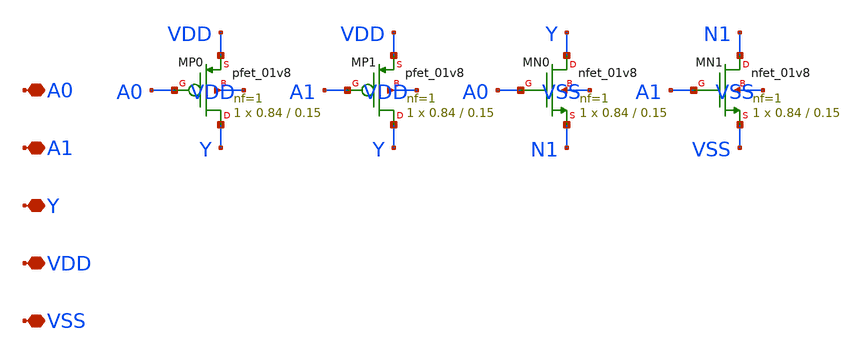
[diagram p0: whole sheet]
** sch_path: design/compiler/cells/sram_nand2.sch
**.subckt sram_nand2 A0 A1 Y VDD VSS
*.iopin A0
*.iopin A1
*.iopin Y
*.iopin VDD
*.iopin VSS
XMP0 Y A0 VDD VDD sky130_fd_pr__pfet_01v8 L=0.15 W=0.84 nf=1 ad=0.2436 as=0.2436 pd=2.26 ps=2.26
+ nrd=0.3452 nrs=0.3452 sa=0 sb=0 sd=0 mult=1 m=1
XMP1 Y A1 VDD VDD sky130_fd_pr__pfet_01v8 L=0.15 W=0.84 nf=1 ad=0.2436 as=0.2436 pd=2.26 ps=2.26
+ nrd=0.3452 nrs=0.3452 sa=0 sb=0 sd=0 mult=1 m=1
XMN0 Y A0 N1 VSS sky130_fd_pr__nfet_01v8 L=0.15 W=0.84 nf=1 ad=0.2436 as=0.2436 pd=2.26 ps=2.26
+ nrd=0.3452 nrs=0.3452 sa=0 sb=0 sd=0 mult=1 m=1
XMN1 N1 A1 VSS VSS sky130_fd_pr__nfet_01v8 L=0.15 W=0.84 nf=1 ad=0.2436 as=0.2436 pd=2.26 ps=2.26
+ nrd=0.3452 nrs=0.3452 sa=0 sb=0 sd=0 mult=1 m=1
**.ends
.end
